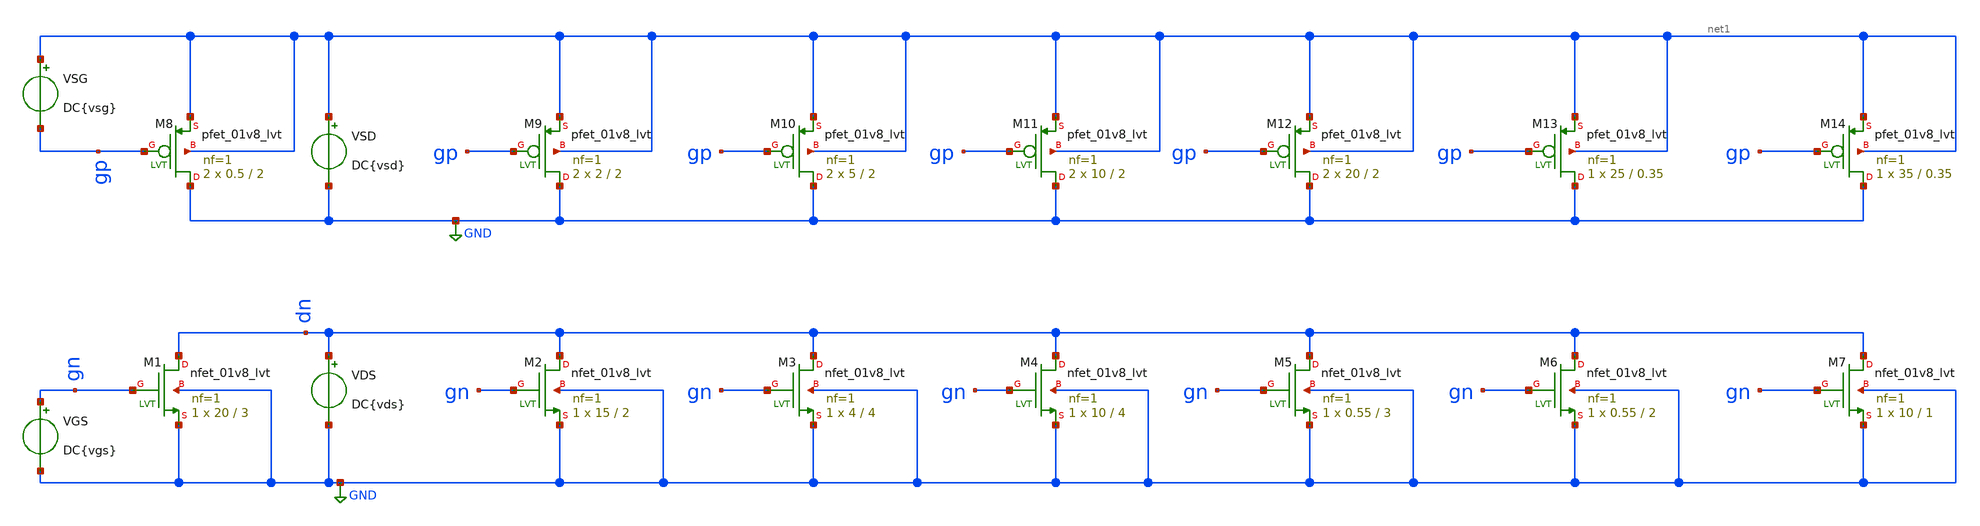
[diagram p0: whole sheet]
** sch_path: XSCHEM/VTH_characterization_lvt_01v8.sch
**.subckt VTH_characterization_lvt_01v8
XM1 dn gn GND GND sky130_fd_pr__nfet_01v8_lvt L=3 W=20 nf=1 ad='int((nf+1)/2) * W/nf * 0.29' as='int((nf+2)/2) * W/nf * 0.29'
+ pd='2*int((nf+1)/2) * (W/nf + 0.29)' ps='2*int((nf+2)/2) * (W/nf + 0.29)' nrd='0.29 / W' nrs='0.29 / W'
+ sa=0 sb=0 sd=0 mult=1 m=1
XM2 dn gn GND GND sky130_fd_pr__nfet_01v8_lvt L=2 W=15 nf=1 ad='int((nf+1)/2) * W/nf * 0.29' as='int((nf+2)/2) * W/nf * 0.29'
+ pd='2*int((nf+1)/2) * (W/nf + 0.29)' ps='2*int((nf+2)/2) * (W/nf + 0.29)' nrd='0.29 / W' nrs='0.29 / W'
+ sa=0 sb=0 sd=0 mult=1 m=1
VGS gn GND DC{vgs}
VDS dn GND DC{vds}
XM3 dn gn GND GND sky130_fd_pr__nfet_01v8_lvt L=4 W=4 nf=1 ad='int((nf+1)/2) * W/nf * 0.29' as='int((nf+2)/2) * W/nf * 0.29'
+ pd='2*int((nf+1)/2) * (W/nf + 0.29)' ps='2*int((nf+2)/2) * (W/nf + 0.29)' nrd='0.29 / W' nrs='0.29 / W'
+ sa=0 sb=0 sd=0 mult=1 m=1
XM4 dn gn GND GND sky130_fd_pr__nfet_01v8_lvt L=4 W=10 nf=1 ad='int((nf+1)/2) * W/nf * 0.29' as='int((nf+2)/2) * W/nf * 0.29'
+ pd='2*int((nf+1)/2) * (W/nf + 0.29)' ps='2*int((nf+2)/2) * (W/nf + 0.29)' nrd='0.29 / W' nrs='0.29 / W'
+ sa=0 sb=0 sd=0 mult=1 m=1
XM5 dn gn GND GND sky130_fd_pr__nfet_01v8_lvt L=3 W=0.55 nf=1 ad='int((nf+1)/2) * W/nf * 0.29' as='int((nf+2)/2) * W/nf * 0.29'
+ pd='2*int((nf+1)/2) * (W/nf + 0.29)' ps='2*int((nf+2)/2) * (W/nf + 0.29)' nrd='0.29 / W' nrs='0.29 / W'
+ sa=0 sb=0 sd=0 mult=1 m=1
XM6 dn gn GND GND sky130_fd_pr__nfet_01v8_lvt L=2 W=0.55 nf=1 ad='int((nf+1)/2) * W/nf * 0.29' as='int((nf+2)/2) * W/nf * 0.29'
+ pd='2*int((nf+1)/2) * (W/nf + 0.29)' ps='2*int((nf+2)/2) * (W/nf + 0.29)' nrd='0.29 / W' nrs='0.29 / W'
+ sa=0 sb=0 sd=0 mult=1 m=1
VSG net1 gp DC{vsg}
VSD net1 GND DC{vsd}
XM7 dn gn GND GND sky130_fd_pr__nfet_01v8_lvt L=1 W=10 nf=1 ad='int((nf+1)/2) * W/nf * 0.29' as='int((nf+2)/2) * W/nf * 0.29'
+ pd='2*int((nf+1)/2) * (W/nf + 0.29)' ps='2*int((nf+2)/2) * (W/nf + 0.29)' nrd='0.29 / W' nrs='0.29 / W'
+ sa=0 sb=0 sd=0 mult=1 m=1
XM8 GND gp net1 net1 sky130_fd_pr__pfet_01v8_lvt L=2 W=0.5 nf=1 ad='int((nf+1)/2) * W/nf * 0.29' as='int((nf+2)/2) * W/nf * 0.29'
+ pd='2*int((nf+1)/2) * (W/nf + 0.29)' ps='2*int((nf+2)/2) * (W/nf + 0.29)' nrd='0.29 / W' nrs='0.29 / W'
+ sa=0 sb=0 sd=0 mult=2 m=2
XM9 GND gp net1 net1 sky130_fd_pr__pfet_01v8_lvt L=2 W=2 nf=1 ad='int((nf+1)/2) * W/nf * 0.29' as='int((nf+2)/2) * W/nf * 0.29'
+ pd='2*int((nf+1)/2) * (W/nf + 0.29)' ps='2*int((nf+2)/2) * (W/nf + 0.29)' nrd='0.29 / W' nrs='0.29 / W'
+ sa=0 sb=0 sd=0 mult=2 m=2
XM10 GND gp net1 net1 sky130_fd_pr__pfet_01v8_lvt L=2 W=5 nf=1 ad='int((nf+1)/2) * W/nf * 0.29' as='int((nf+2)/2) * W/nf * 0.29'
+ pd='2*int((nf+1)/2) * (W/nf + 0.29)' ps='2*int((nf+2)/2) * (W/nf + 0.29)' nrd='0.29 / W' nrs='0.29 / W'
+ sa=0 sb=0 sd=0 mult=2 m=2
XM11 GND gp net1 net1 sky130_fd_pr__pfet_01v8_lvt L=2 W=10 nf=1 ad='int((nf+1)/2) * W/nf * 0.29' as='int((nf+2)/2) * W/nf * 0.29'
+ pd='2*int((nf+1)/2) * (W/nf + 0.29)' ps='2*int((nf+2)/2) * (W/nf + 0.29)' nrd='0.29 / W' nrs='0.29 / W'
+ sa=0 sb=0 sd=0 mult=2 m=2
XM12 GND gp net1 net1 sky130_fd_pr__pfet_01v8_lvt L=2 W=20 nf=1 ad='int((nf+1)/2) * W/nf * 0.29' as='int((nf+2)/2) * W/nf * 0.29'
+ pd='2*int((nf+1)/2) * (W/nf + 0.29)' ps='2*int((nf+2)/2) * (W/nf + 0.29)' nrd='0.29 / W' nrs='0.29 / W'
+ sa=0 sb=0 sd=0 mult=2 m=2
XM13 GND gp net1 net1 sky130_fd_pr__pfet_01v8_lvt L=0.35 W=25 nf=1 ad='int((nf+1)/2) * W/nf * 0.29' as='int((nf+2)/2) * W/nf * 0.29'
+ pd='2*int((nf+1)/2) * (W/nf + 0.29)' ps='2*int((nf+2)/2) * (W/nf + 0.29)' nrd='0.29 / W' nrs='0.29 / W'
+ sa=0 sb=0 sd=0 mult=1 m=1
XM14 GND gp net1 net1 sky130_fd_pr__pfet_01v8_lvt L=0.35 W=35 nf=1 ad='int((nf+1)/2) * W/nf * 0.29' as='int((nf+2)/2) * W/nf * 0.29'
+ pd='2*int((nf+1)/2) * (W/nf + 0.29)' ps='2*int((nf+2)/2) * (W/nf + 0.29)' nrd='0.29 / W' nrs='0.29 / W'
+ sa=0 sb=0 sd=0 mult=1 m=1
**** begin user architecture code



* Parameters
.param vds = 1.8
.param vgs = 0.9
.param vsd = 1.8
.param vsg = 0.9
.options TEMPS = 27.0

* Models
.lib /home/karlajcm/skywater130/skywater-pdk/libraries/sky130_fd_pr/latest/models/sky130.lib.spice TT

* Data to save
.save all  @M.XM1.msky130_fd_pr__nfet_01v8_lvt[id]  @M.XM1.msky130_fd_pr__nfet_01v8_lvt[gm]  @M.XM1.msky130_fd_pr__nfet_01v8_lvt[vth]  @M.XM1.msky130_fd_pr__nfet_01v8_lvt[vds]  @M.XM1.msky130_fd_pr__nfet_01v8_lvt[vdsat]  @M.XM1.msky130_fd_pr__nfet_01v8_lvt[vgs]  @M.XM1.msky130_fd_pr__nfet_01v8_lvt[cgg]  @M.XM2.msky130_fd_pr__nfet_01v8_lvt[id]  @M.XM2.msky130_fd_pr__nfet_01v8_lvt[gm]  @M.XM2.msky130_fd_pr__nfet_01v8_lvt[vth]  @M.XM2.msky130_fd_pr__nfet_01v8_lvt[vds]  @M.XM2.msky130_fd_pr__nfet_01v8_lvt[vdsat]  @M.XM2.msky130_fd_pr__nfet_01v8_lvt[vgs]  @M.XM2.msky130_fd_pr__nfet_01v8_lvt[cgg]  @M.XM3.msky130_fd_pr__nfet_01v8_lvt[id]  @M.XM3.msky130_fd_pr__nfet_01v8_lvt[gm]  @M.XM3.msky130_fd_pr__nfet_01v8_lvt[vth]  @M.XM3.msky130_fd_pr__nfet_01v8_lvt[vds]  @M.XM3.msky130_fd_pr__nfet_01v8_lvt[vdsat]  @M.XM3.msky130_fd_pr__nfet_01v8_lvt[vgs]  @M.XM3.msky130_fd_pr__nfet_01v8_lvt[cgg]  @M.XM4.msky130_fd_pr__nfet_01v8_lvt[id]  @M.XM4.msky130_fd_pr__nfet_01v8_lvt[gm]  @M.XM4.msky130_fd_pr__nfet_01v8_lvt[vth]  @M.XM4.msky130_fd_pr__nfet_01v8_lvt[vds]  @M.XM4.msky130_fd_pr__nfet_01v8_lvt[vdsat]  @M.XM4.msky130_fd_pr__nfet_01v8_lvt[vgs]  @M.XM4.msky130_fd_pr__nfet_01v8_lvt[cgg]  @M.XM5.msky130_fd_pr__nfet_01v8_lvt[id]  @M.XM5.msky130_fd_pr__nfet_01v8_lvt[gm]  @M.XM5.msky130_fd_pr__nfet_01v8_lvt[vth]  @M.XM5.msky130_fd_pr__nfet_01v8_lvt[vds]  @M.XM5.msky130_fd_pr__nfet_01v8_lvt[vdsat]  @M.XM5.msky130_fd_pr__nfet_01v8_lvt[vgs]  @M.XM5.msky130_fd_pr__nfet_01v8_lvt[cgg]  @M.XM6.msky130_fd_pr__nfet_01v8_lvt[id]  @M.XM6.msky130_fd_pr__nfet_01v8_lvt[gm]  @M.XM6.msky130_fd_pr__nfet_01v8_lvt[vth]  @M.XM6.msky130_fd_pr__nfet_01v8_lvt[vds]  @M.XM6.msky130_fd_pr__nfet_01v8_lvt[vdsat]  @M.XM6.msky130_fd_pr__nfet_01v8_lvt[vgs]  @M.XM6.msky130_fd_pr__nfet_01v8_lvt[cgg]  @M.XM7.msky130_fd_pr__nfet_01v8_lvt[id]  @M.XM7.msky130_fd_pr__nfet_01v8_lvt[gm]  @M.XM7.msky130_fd_pr__nfet_01v8_lvt[vth]  @M.XM7.msky130_fd_pr__nfet_01v8_lvt[vds]  @M.XM7.msky130_fd_pr__nfet_01v8_lvt[vdsat]  @M.XM7.msky130_fd_pr__nfet_01v8_lvt[vgs]  @M.XM7.msky130_fd_pr__nfet_01v8_lvt[cgg]  @M.XM8.msky130_fd_pr__pfet_01v8_lvt[id]  @M.XM8.msky130_fd_pr__pfet_01v8_lvt[gm]  @M.XM8.msky130_fd_pr__pfet_01v8_lvt[vth]  @M.XM8.msky130_fd_pr__pfet_01v8_lvt[vds]  @M.XM8.msky130_fd_pr__pfet_01v8_lvt[vdsat]  @M.XM8.msky130_fd_pr__pfet_01v8_lvt[vgs]  @M.XM8.msky130_fd_pr__pfet_01v8_lvt[cgg]  @M.XM9.msky130_fd_pr__pfet_01v8_lvt[id]  @M.XM9.msky130_fd_pr__pfet_01v8_lvt[gm]  @M.XM9.msky130_fd_pr__pfet_01v8_lvt[vth]  @M.XM9.msky130_fd_pr__pfet_01v8_lvt[vds]  @M.XM9.msky130_fd_pr__pfet_01v8_lvt[vdsat]  @M.XM9.msky130_fd_pr__pfet_01v8_lvt[vgs]  @M.XM9.msky130_fd_pr__pfet_01v8_lvt[cgg]  @M.XM10.msky130_fd_pr__pfet_01v8_lvt[id]  @M.XM10.msky130_fd_pr__pfet_01v8_lvt[gm]  @M.XM10.msky130_fd_pr__pfet_01v8_lvt[vth]  @M.XM10.msky130_fd_pr__pfet_01v8_lvt[vds]  @M.XM10.msky130_fd_pr__pfet_01v8_lvt[vdsat]  @M.XM10.msky130_fd_pr__pfet_01v8_lvt[vgs]  @M.XM10.msky130_fd_pr__pfet_01v8_lvt[cgg]  @M.XM11.msky130_fd_pr__pfet_01v8_lvt[id]  @M.XM11.msky130_fd_pr__pfet_01v8_lvt[gm]  @M.XM11.msky130_fd_pr__pfet_01v8_lvt[vth]  @M.XM11.msky130_fd_pr__pfet_01v8_lvt[vds]  @M.XM11.msky130_fd_pr__pfet_01v8_lvt[vdsat]  @M.XM11.msky130_fd_pr__pfet_01v8_lvt[vgs]  @M.XM11.msky130_fd_pr__pfet_01v8_lvt[cgg]  @M.XM12.msky130_fd_pr__pfet_01v8_lvt[id]  @M.XM12.msky130_fd_pr__pfet_01v8_lvt[gm]  @M.XM12.msky130_fd_pr__pfet_01v8_lvt[vth]  @M.XM12.msky130_fd_pr__pfet_01v8_lvt[vds]  @M.XM12.msky130_fd_pr__pfet_01v8_lvt[vdsat]  @M.XM12.msky130_fd_pr__pfet_01v8_lvt[vgs]  @M.XM12.msky130_fd_pr__pfet_01v8_lvt[cgg]  @M.XM13.msky130_fd_pr__pfet_01v8_lvt[id]  @M.XM13.msky130_fd_pr__pfet_01v8_lvt[gm]  @M.XM13.msky130_fd_pr__pfet_01v8_lvt[vth]  @M.XM13.msky130_fd_pr__pfet_01v8_lvt[vds]  @M.XM13.msky130_fd_pr__pfet_01v8_lvt[vdsat]  @M.XM13.msky130_fd_pr__pfet_01v8_lvt[vgs]  @M.XM13.msky130_fd_pr__pfet_01v8_lvt[cgg]  @M.XM14.msky130_fd_pr__pfet_01v8_lvt[id]  @M.XM14.msky130_fd_pr__pfet_01v8_lvt[gm]  @M.XM14.msky130_fd_pr__pfet_01v8_lvt[vth]  @M.XM14.msky130_fd_pr__pfet_01v8_lvt[vds]  @M.XM14.msky130_fd_pr__pfet_01v8_lvt[vdsat]  @M.XM14.msky130_fd_pr__pfet_01v8_lvt[vgs]  @M.XM14.msky130_fd_pr__pfet_01v8_lvt[cgg]

* Simulation
.control
  dc VDS 0 1.8 0.01 VGS 0 1.8 0.3 VSD 0 1.8 0.01 VSG 0 1.8 0.3
  setplot dc1
  plot @M.XM1.msky130_fd_pr__nfet_01v8_lvt[id] @M.XM2.msky130_fd_pr__nfet_01v8_lvt[id] @M.XM3.msky130_fd_pr__nfet_01v8_lvt[id]
+ @M.XM4.msky130_fd_pr__nfet_01v8_lvt[id] @M.XM5.msky130_fd_pr__nfet_01v8_lvt[id] @M.XM6.msky130_fd_pr__nfet_01v8_lvt[id]
+ @M.XM7.msky130_fd_pr__nfet_01v8_lvt[id] ylabel Id xlabel Vds title 'NMOS: Id vs Vds vs Vgs'
  plot @M.XM8.msky130_fd_pr__pfet_01v8_lvt[id] @M.XM9.msky130_fd_pr__pfet_01v8_lvt[id] @M.XM10.msky130_fd_pr__pfet_01v8_lvt[id]
+ @M.XM11.msky130_fd_pr__pfet_01v8_lvt[id] @M.XM12.msky130_fd_pr__pfet_01v8_lvt[id] @M.XM13.msky130_fd_pr__pfet_01v8_lvt[id]
+ @M.XM14.msky130_fd_pr__pfet_01v8_lvt[id] ylabel Id xlabel Vsd title 'PMOS:Id vs Vsd vs Vsg'
  set filetype = ascii
  write VTH_characterization_lvt_01v8_dc1.raw

  *alterparam vds = 0
  *alterparam vsd = 0
  *reset
  *dc VGS -1.8 1.8 0.01 VSG -1.8 1.8 0.01
  *setplot dc2
  *plot @M.XM1.msky130_fd_pr__nfet_01v8_lvt[cgg] @M.XM2.msky130_fd_pr__nfet_01v8_lvt[cgg] @M.XM3.msky130_fd_pr__nfet_01v8_lvt[cgg]
+ @M.XM4.msky130_fd_pr__nfet_01v8_lvt[cgg] @M.XM5.msky130_fd_pr__nfet_01v8_lvt[cgg] @M.XM6.msky130_fd_pr__nfet_01v8_lvt[cgg]
+ @M.XM7.msky130_fd_pr__nfet_01v8_lvt[cgg] ylabel Cgg xlabel Vgs title 'NMOS:Cgg vs Vgs'
  *plot @M.XM8.msky130_fd_pr__pfet_01v8_lvt[cgg] @M.XM9.msky130_fd_pr__pfet_01v8_lvt[cgg] @M.XM10.msky130_fd_pr__pfet_01v8_lvt[cgg]
+ @M.XM11.msky130_fd_pr__pfet_01v8_lvt[cgg] @M.XM12.msky130_fd_pr__pfet_01v8_lvt[cgg] @M.XM13.msky130_fd_pr__pfet_01v8_lvt[cgg]
+ @M.XM14.msky130_fd_pr__pfet_01v8_lvt[cgg] ylabel Cgg xlabel Vgs title 'PMOS:Cgg vs Vsg'
  *set filetype = ascii
  *write VTH_characterization_lvt_01v8_dc2.raw

  *reset
  *dc VGS -1.8 1.8 0.01 VSG -1.8 1.8 0.01
  *setplot dc3
  *plot @M.XM1.msky130_fd_pr__nfet_01v8_lvt[vth] @M.XM2.msky130_fd_pr__nfet_01v8_lvt[vth] @M.XM3.msky130_fd_pr__nfet_01v8_lvt[vth]
+ @M.XM4.msky130_fd_pr__nfet_01v8_lvt[vth] @M.XM5.msky130_fd_pr__nfet_01v8_lvt[vth] @M.XM6.msky130_fd_pr__nfet_01v8_lvt[vth]
+ @M.XM7.msky130_fd_pr__nfet_01v8_lvt[vth] ylabel Vth xlabel Vgs title 'NMOS:Vth vs Vgs'
  *plot @M.XM8.msky130_fd_pr__pfet_01v8_lvt[vth] @M.XM9.msky130_fd_pr__pfet_01v8_lvt[vth] @M.XM10.msky130_fd_pr__pfet_01v8_lvt[vth]
+ @M.XM11.msky130_fd_pr__pfet_01v8_lvt[vth] @M.XM12.msky130_fd_pr__pfet_01v8_lvt[vth] @M.XM13.msky130_fd_pr__pfet_01v8_lvt[vth]
+ @M.XM14.msky130_fd_pr__pfet_01v8_lvt[vth] ylabel Vth xlabel Vsg title 'PMOS:Vth vs Vsg'
  *set filetype = ascii
  *write VTH_characterization_lvt_01v8_dc3.raw

  reset
  unset filetype
  op
  save all
  write VTH_characterization_lvt_01v8.raw

.endc

.end


**** end user architecture code
**.ends
.GLOBAL GND
.end
